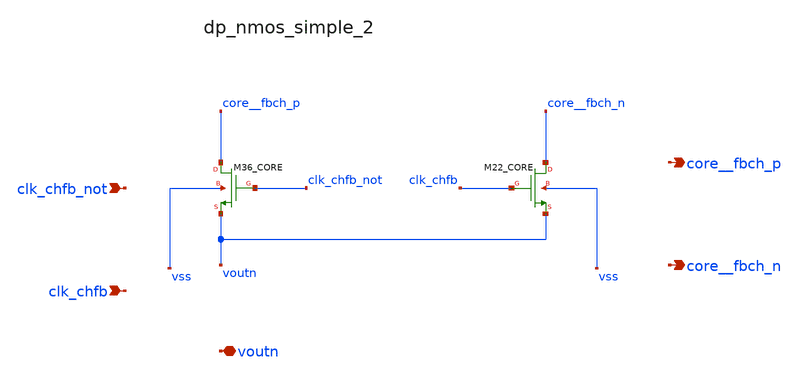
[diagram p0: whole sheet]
** sch_path: analog-db/raw/ia_006_fan_chopper_cmfb/hier/blocks/dp_nmos_simple_2.sch
**.subckt dp_nmos_simple_2 clk_chfb_not clk_chfb voutn core__fbch_p core__fbch_n
*.ipin clk_chfb_not
*.ipin clk_chfb
*.iopin voutn
*.opin core__fbch_p
*.opin core__fbch_n
XM22_CORE core__fbch_n clk_chfb voutn vss sg13_lv_nmos w=x_dut_xm22_core_w l=x_dut_xm22_core_l ng=1
+ m=x_dut_xm22_core_m
XM36_CORE core__fbch_p clk_chfb_not voutn vss sg13_lv_nmos w=x_dut_xm36_core_w l=x_dut_xm36_core_l
+ ng=1 m=x_dut_xm36_core_m
**.ends
.end
